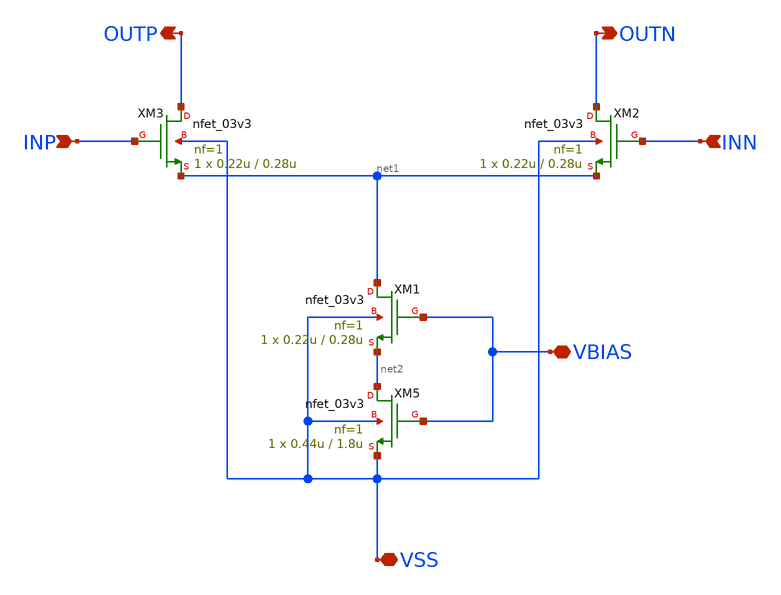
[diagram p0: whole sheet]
** sch_path: xschem/CS_Switch_2x2.sch
**.subckt CS_Switch_2x2 INP INN OUTP OUTN VBIAS VSS
*.ipin INP
*.ipin INN
*.opin OUTP
*.opin OUTN
*.iopin VBIAS
*.iopin VSS
XM1 net1 VBIAS net2 VSS nfet_03v3 L=0.28u W=0.22u nf=1 ad='int((nf+1)/2) * W/nf * 0.18u' as='int((nf+2)/2) * W/nf * 0.18u'
+ pd='2*int((nf+1)/2) * (W/nf + 0.18u)' ps='2*int((nf+2)/2) * (W/nf + 0.18u)' nrd='0.18u / W' nrs='0.18u / W'
+ sa=0 sb=0 sd=0 m=1
XM2 OUTN INN net1 VSS nfet_03v3 L=0.28u W=0.22u nf=1 ad='int((nf+1)/2) * W/nf * 0.18u' as='int((nf+2)/2) * W/nf * 0.18u'
+ pd='2*int((nf+1)/2) * (W/nf + 0.18u)' ps='2*int((nf+2)/2) * (W/nf + 0.18u)' nrd='0.18u / W' nrs='0.18u / W'
+ sa=0 sb=0 sd=0 m=1
XM3 OUTP INP net1 VSS nfet_03v3 L=0.28u W=0.22u nf=1 ad='int((nf+1)/2) * W/nf * 0.18u' as='int((nf+2)/2) * W/nf * 0.18u'
+ pd='2*int((nf+1)/2) * (W/nf + 0.18u)' ps='2*int((nf+2)/2) * (W/nf + 0.18u)' nrd='0.18u / W' nrs='0.18u / W'
+ sa=0 sb=0 sd=0 m=1
XM5 net2 VBIAS VSS VSS nfet_03v3 L=1.8u W=0.44u nf=1 ad='int((nf+1)/2) * W/nf * 0.18u' as='int((nf+2)/2) * W/nf * 0.18u'
+ pd='2*int((nf+1)/2) * (W/nf + 0.18u)' ps='2*int((nf+2)/2) * (W/nf + 0.18u)' nrd='0.18u / W' nrs='0.18u / W'
+ sa=0 sb=0 sd=0 m=1
**.ends
.end
